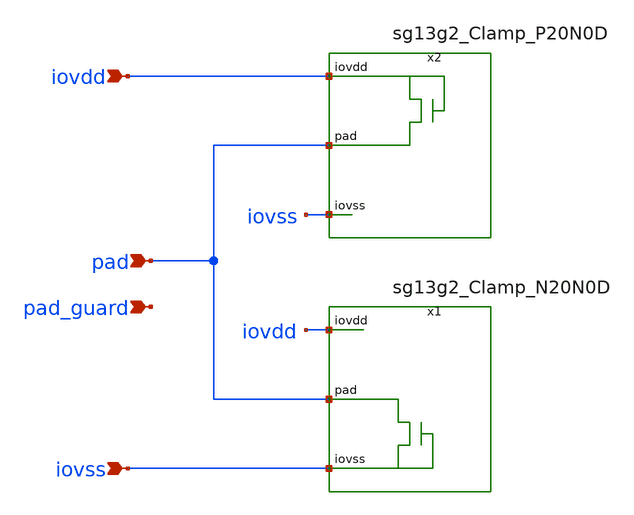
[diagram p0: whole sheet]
** sch_path: trident_test_structures/design_data/xschem/IOPadAnalog_submodules/clamps.sch
**.subckt clamps iovdd iovss pad pad_guard
*.ipin iovdd
*.ipin iovss
*.ipin pad
*.ipin pad_guard
x1 iovss iovdd pad sg13g2_Clamp_N20N0D
x2 iovss iovdd pad sg13g2_Clamp_P20N0D
**.ends
.end
